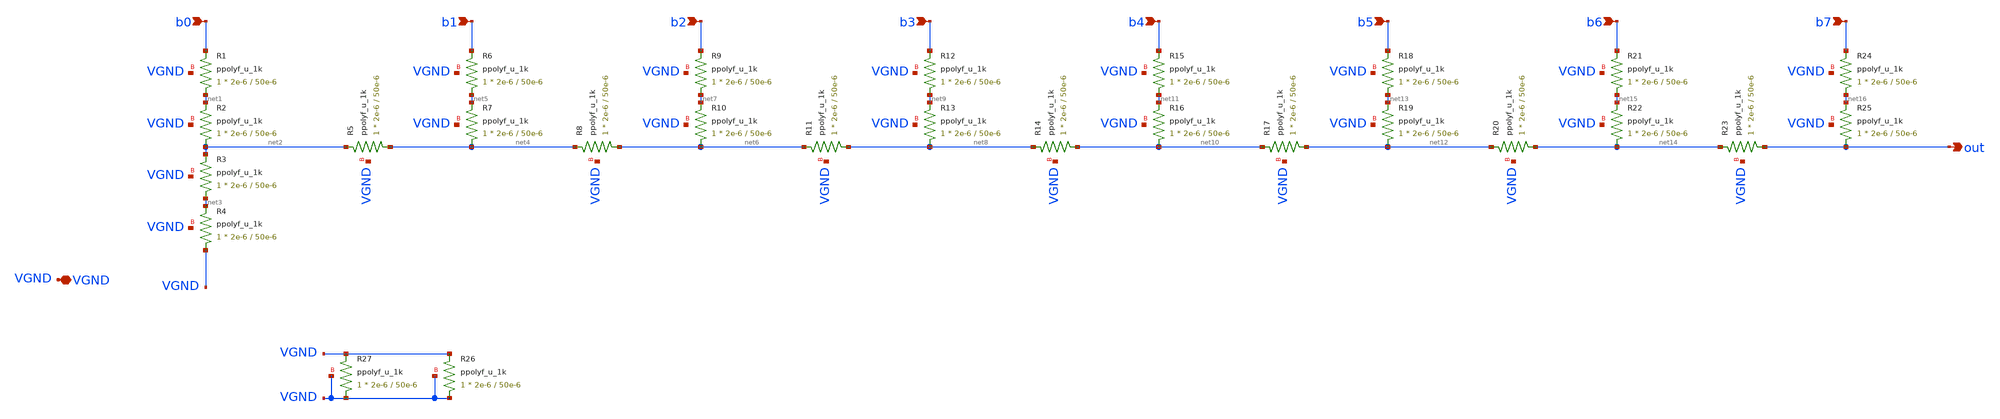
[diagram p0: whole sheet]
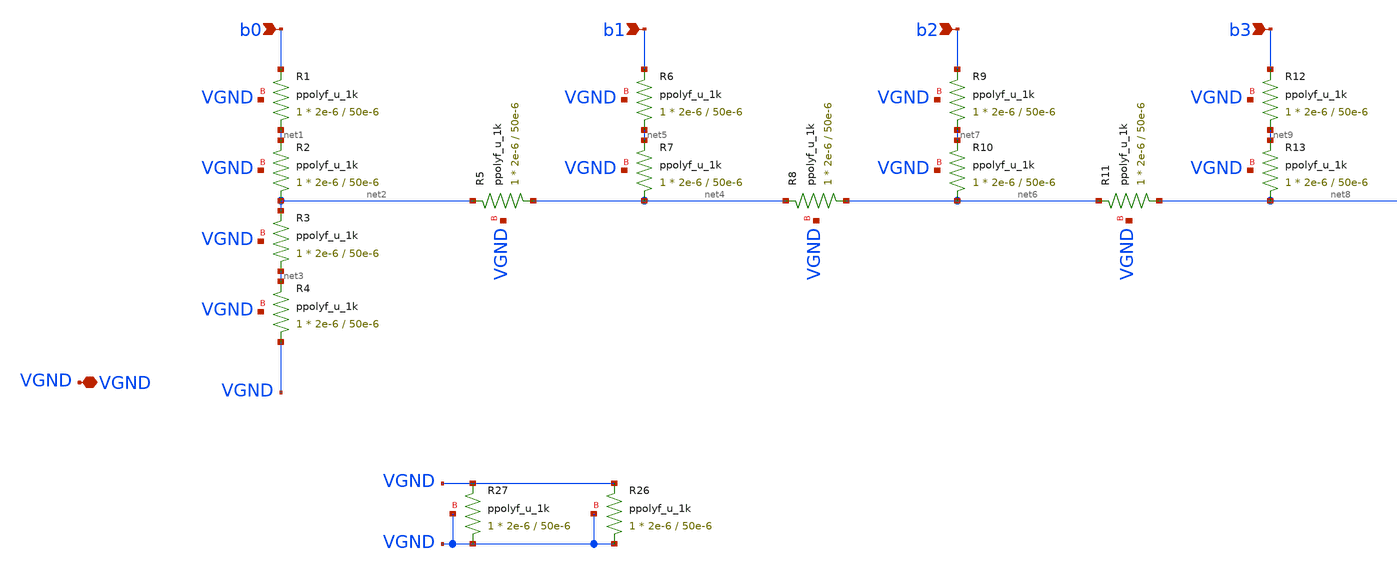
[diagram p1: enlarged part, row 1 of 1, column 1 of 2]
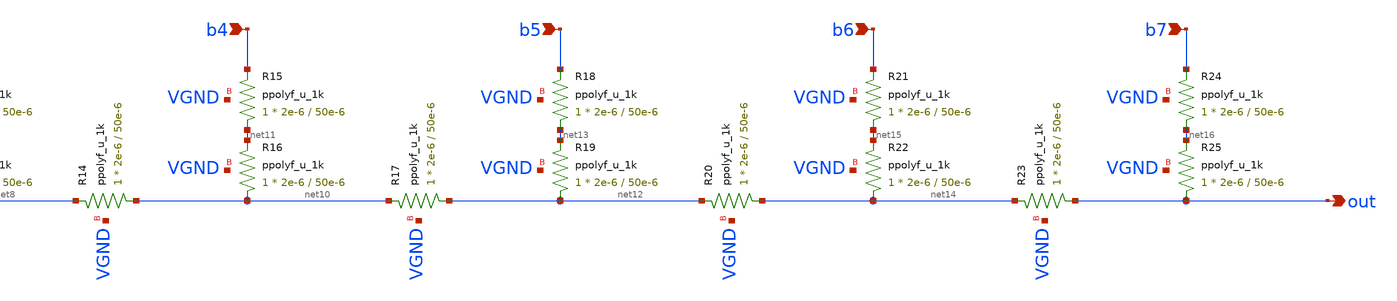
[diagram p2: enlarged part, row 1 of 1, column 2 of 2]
** sch_path: xschem/r2r.sch
**.subckt r2r VGND b0 b1 out b2 b3 b4 b5 b6 b7
*.iopin VGND
*.ipin b0
*.ipin b1
*.opin out
*.ipin b2
*.ipin b3
*.ipin b4
*.ipin b5
*.ipin b6
*.ipin b7
XR1 net1 b0 VGND ppolyf_u_1k r_width=2e-6 r_length=50e-6 m=1
XR2 net2 net1 VGND ppolyf_u_1k r_width=2e-6 r_length=50e-6 m=1
XR3 net3 net2 VGND ppolyf_u_1k r_width=2e-6 r_length=50e-6 m=1
XR4 VGND net3 VGND ppolyf_u_1k r_width=2e-6 r_length=50e-6 m=1
XR5 net4 net2 VGND ppolyf_u_1k r_width=2e-6 r_length=50e-6 m=1
XR6 net5 b1 VGND ppolyf_u_1k r_width=2e-6 r_length=50e-6 m=1
XR7 net4 net5 VGND ppolyf_u_1k r_width=2e-6 r_length=50e-6 m=1
XR8 net6 net4 VGND ppolyf_u_1k r_width=2e-6 r_length=50e-6 m=1
XR9 net7 b2 VGND ppolyf_u_1k r_width=2e-6 r_length=50e-6 m=1
XR10 net6 net7 VGND ppolyf_u_1k r_width=2e-6 r_length=50e-6 m=1
XR11 net8 net6 VGND ppolyf_u_1k r_width=2e-6 r_length=50e-6 m=1
XR12 net9 b3 VGND ppolyf_u_1k r_width=2e-6 r_length=50e-6 m=1
XR13 net8 net9 VGND ppolyf_u_1k r_width=2e-6 r_length=50e-6 m=1
XR14 net10 net8 VGND ppolyf_u_1k r_width=2e-6 r_length=50e-6 m=1
XR15 net11 b4 VGND ppolyf_u_1k r_width=2e-6 r_length=50e-6 m=1
XR16 net10 net11 VGND ppolyf_u_1k r_width=2e-6 r_length=50e-6 m=1
XR17 net12 net10 VGND ppolyf_u_1k r_width=2e-6 r_length=50e-6 m=1
XR18 net13 b5 VGND ppolyf_u_1k r_width=2e-6 r_length=50e-6 m=1
XR19 net12 net13 VGND ppolyf_u_1k r_width=2e-6 r_length=50e-6 m=1
XR20 net14 net12 VGND ppolyf_u_1k r_width=2e-6 r_length=50e-6 m=1
XR21 net15 b6 VGND ppolyf_u_1k r_width=2e-6 r_length=50e-6 m=1
XR22 net14 net15 VGND ppolyf_u_1k r_width=2e-6 r_length=50e-6 m=1
XR23 out net14 VGND ppolyf_u_1k r_width=2e-6 r_length=50e-6 m=1
XR24 net16 b7 VGND ppolyf_u_1k r_width=2e-6 r_length=50e-6 m=1
XR25 out net16 VGND ppolyf_u_1k r_width=2e-6 r_length=50e-6 m=1
XR26 VGND VGND VGND ppolyf_u_1k r_width=2e-6 r_length=50e-6 m=1
XR27 VGND VGND VGND ppolyf_u_1k r_width=2e-6 r_length=50e-6 m=1
**.ends
.end
